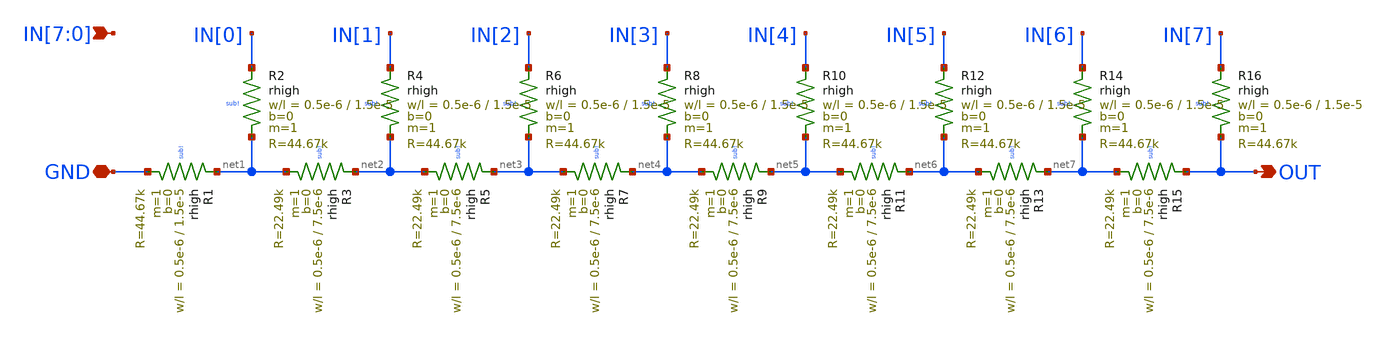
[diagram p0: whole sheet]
** sch_path: xschem/r2r_dac_combined.sch
**.subckt r2r_dac_combined GND IN[7],IN[6],IN[5],IN[4],IN[3],IN[2],IN[1],IN[0] OUT
*.iopin GND
*.ipin IN[7],IN[6],IN[5],IN[4],IN[3],IN[2],IN[1],IN[0]
*.opin OUT
XR1 net1 GND sub! rhigh w=0.5e-6 l=1.5e-5 m=1 b=0 mm_ok=1
XR2 IN[0] net1 sub! rhigh w=0.5e-6 l=1.5e-5 m=1 b=0 mm_ok=1
XR3 net2 net1 sub! rhigh w=0.5e-6 l=7.5e-6 m=1 b=0 mm_ok=1
XR4 IN[1] net2 sub! rhigh w=0.5e-6 l=1.5e-5 m=1 b=0 mm_ok=1
XR5 net3 net2 sub! rhigh w=0.5e-6 l=7.5e-6 m=1 b=0 mm_ok=1
XR6 IN[2] net3 sub! rhigh w=0.5e-6 l=1.5e-5 m=1 b=0 mm_ok=1
XR7 net4 net3 sub! rhigh w=0.5e-6 l=7.5e-6 m=1 b=0 mm_ok=1
XR8 IN[3] net4 sub! rhigh w=0.5e-6 l=1.5e-5 m=1 b=0 mm_ok=1
XR9 net5 net4 sub! rhigh w=0.5e-6 l=7.5e-6 m=1 b=0 mm_ok=1
XR10 IN[4] net5 sub! rhigh w=0.5e-6 l=1.5e-5 m=1 b=0 mm_ok=1
XR11 net6 net5 sub! rhigh w=0.5e-6 l=7.5e-6 m=1 b=0 mm_ok=1
XR12 IN[5] net6 sub! rhigh w=0.5e-6 l=1.5e-5 m=1 b=0 mm_ok=1
XR13 net7 net6 sub! rhigh w=0.5e-6 l=7.5e-6 m=1 b=0 mm_ok=1
XR14 IN[6] net7 sub! rhigh w=0.5e-6 l=1.5e-5 m=1 b=0 mm_ok=1
XR15 OUT net7 sub! rhigh w=0.5e-6 l=7.5e-6 m=1 b=0 mm_ok=1
XR16 IN[7] OUT sub! rhigh w=0.5e-6 l=1.5e-5 m=1 b=0 mm_ok=1
**.ends
.end
